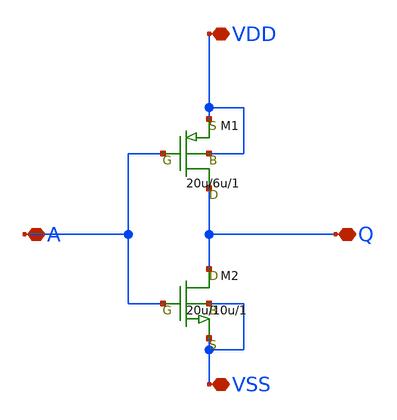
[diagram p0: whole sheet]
** sch_path: member_project/Hizuki1030/my-inverter-lsi/inverter.sch
**.subckt inverter A Q VDD VSS
*.iopin A
*.iopin Q
*.iopin VDD
*.iopin VSS
M1 Q A VDD VDD pmos w=20u l=6u as=0 ps=0 ad=0 pd=0 m=1
M2 Q A VSS VSS nmos w=20u l=10u as=0 ps=0 ad=0 pd=0 m=1
**.ends
.end
